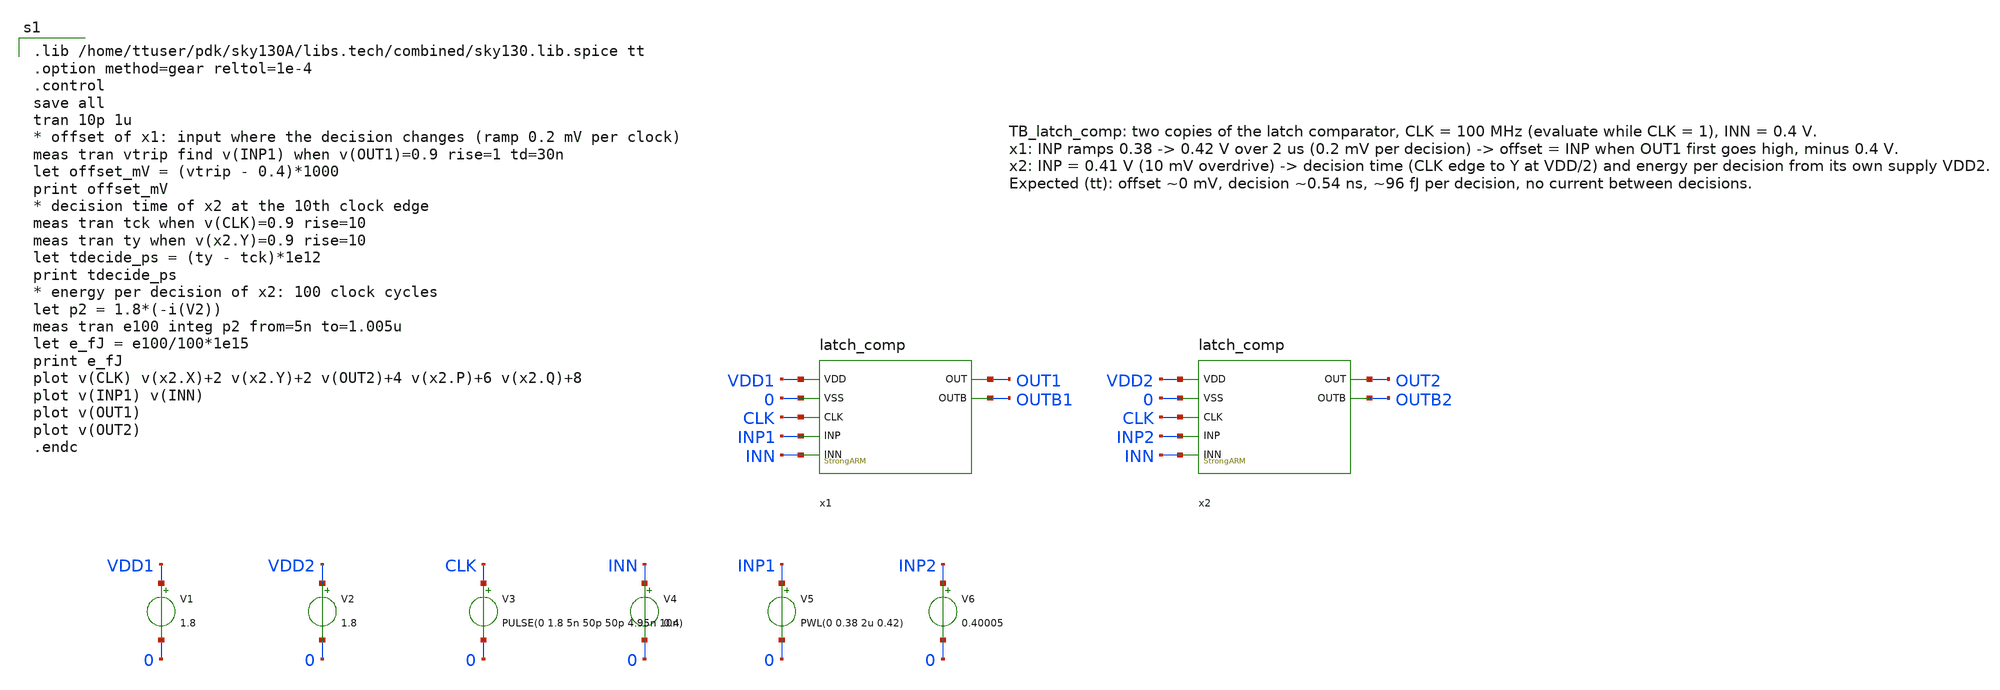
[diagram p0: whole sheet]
** sch_path: SAR_improved/TB_latch_comp.sch
**.subckt TB_latch_comp
x1 VDD1 0 CLK INP1 INN OUT1 OUTB1 latch_comp
x2 VDD2 0 CLK INP2 INN OUT2 OUTB2 latch_comp
V1 VDD1 0 1.8
V2 VDD2 0 1.8
V3 CLK 0 PULSE(0 1.8 5n 50p 50p 4.95n 10n)
V4 INN 0 0.4
V5 INP1 0 PWL(0 0.38 2u 0.42)
V6 INP2 0 0.40005
**** begin user architecture code

.lib /home/ttuser/pdk/sky130A/libs.tech/combined/sky130.lib.spice tt
.option method=gear reltol=1e-4
.control
save all
tran 10p 1u
* offset of x1: input where the decision changes (ramp 0.2 mV per clock)
meas tran vtrip find v(INP1) when v(OUT1)=0.9 rise=1 td=30n
let offset_mV = (vtrip - 0.4)*1000
print offset_mV
* decision time of x2 at the 10th clock edge
meas tran tck when v(CLK)=0.9 rise=10
meas tran ty when v(x2.Y)=0.9 rise=10
let tdecide_ps = (ty - tck)*1e12
print tdecide_ps
* energy per decision of x2: 100 clock cycles
let p2 = 1.8*(-i(V2))
meas tran e100 integ p2 from=5n to=1.005u
let e_fJ = e100/100*1e15
print e_fJ
plot v(CLK) v(x2.X)+2 v(x2.Y)+2 v(OUT2)+4 v(x2.P)+6 v(x2.Q)+8
plot v(INP1) v(INN)
plot v(OUT1)
plot v(OUT2)
.endc

**** end user architecture code
**.ends
.end
